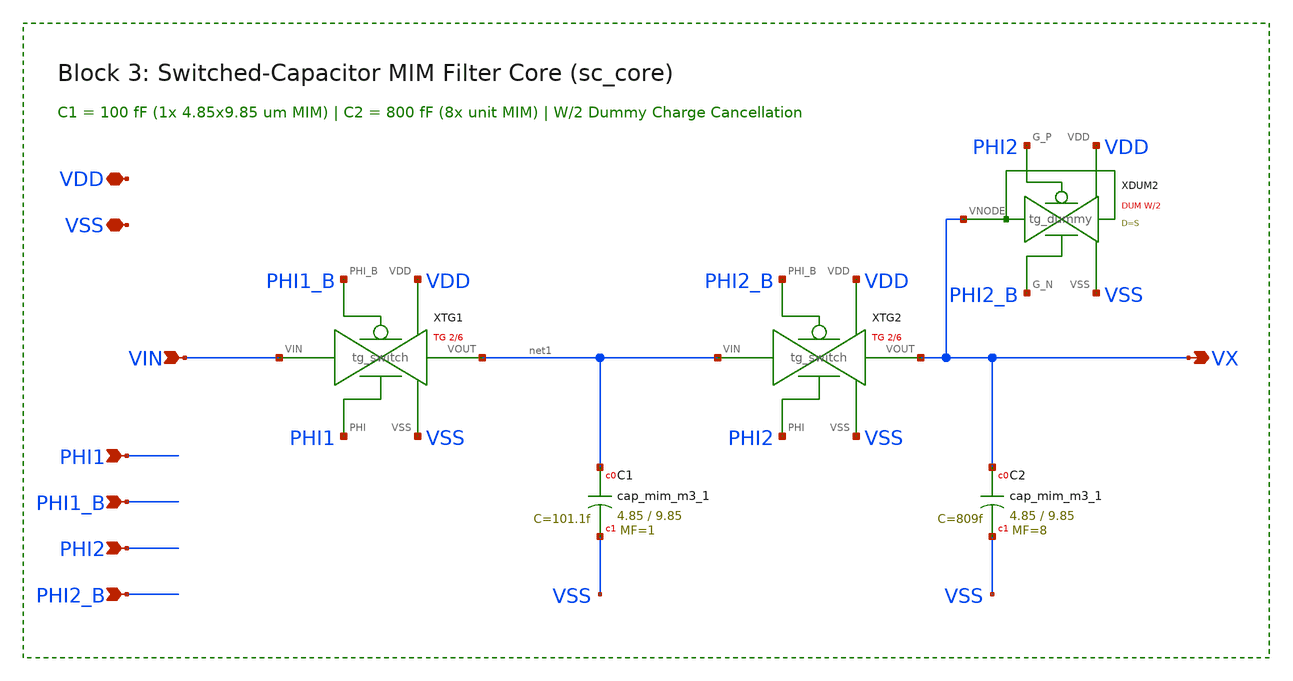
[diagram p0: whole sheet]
** sch_path: sky130-sc-lpf/xschem/sc_core.sch
**.subckt sc_core VDD VSS PHI1 PHI1_B PHI2 PHI2_B VIN VX
*.iopin VDD
*.iopin VSS
*.ipin PHI1
*.ipin PHI1_B
*.ipin PHI2
*.ipin PHI2_B
*.ipin VIN
*.opin VX
XTG1 VIN net1 PHI1 PHI1_B VDD VSS tg_switch
XC1 net1 VSS sky130_fd_pr__cap_mim_m3_1 W=4.85 L=9.85 MF=1 m=1
XTG2 net1 VX PHI2 PHI2_B VDD VSS tg_switch
XC2 VX VSS sky130_fd_pr__cap_mim_m3_1 W=4.85 L=9.85 MF=8 m=8
XDUM2 VX PHI2_B PHI2 VDD VSS tg_dummy
**.ends

* expanding   symbol:  tg_switch.sym # of pins=6
** sym_path: sky130-sc-lpf/xschem/tg_switch.sym
** sch_path: sky130-sc-lpf/xschem/tg_switch.sch
.subckt tg_switch VIN VOUT PHI PHI_B VDD VSS
*.iopin VIN
*.iopin VOUT
*.ipin PHI_B
*.ipin PHI
*.iopin VDD
*.iopin VSS
XMP VOUT PHI_B VIN VDD sky130_fd_pr__pfet_01v8 L=0.15 W=6.0 nf=2 ad='int((nf+1)/2) * W/nf * 0.29' as='int((nf+2)/2) * W/nf * 0.29'
+ pd='2*int((nf+1)/2) * (W/nf + 0.29)' ps='2*int((nf+2)/2) * (W/nf + 0.29)' nrd='0.29 / W' nrs='0.29 / W'
+ sa=0 sb=0 sd=0 mult=1 m=1
XMN VOUT PHI VIN VSS sky130_fd_pr__nfet_01v8 L=0.15 W=2.0 nf=1 ad='int((1 + 1)/2) * 2.0 / 1 * 0.29' as='int((1 + 2)/2) * 2.0 / 1 * 0.29'
+ pd='2*int((1 + 1)/2) * (2.0 / 1 + 0.29)' ps='2*int((1 + 2)/2) * (2.0 / 1 + 0.29)' nrd='0.29 / 2.0 ' nrs='0.29 / 2.0 '
+ sa=0 sb=0 sd=0 mult=1 m=1
.ends


* expanding   symbol:  tg_dummy.sym # of pins=5
** sym_path: sky130-sc-lpf/xschem/tg_dummy.sym
** sch_path: sky130-sc-lpf/xschem/tg_dummy.sch
.subckt tg_dummy VNODE G_N G_P VDD VSS
*.iopin VNODE
*.ipin G_P
*.ipin G_N
*.iopin VDD
*.iopin VSS
XMPD VNODE G_P VNODE VDD sky130_fd_pr__pfet_01v8 L=0.15 W=3.0 nf=1 ad='int((nf+1)/2) * W/nf * 0.29' as='int((nf+2)/2) * W/nf * 0.29'
+ pd='2*int((nf+1)/2) * (W/nf + 0.29)' ps='2*int((nf+2)/2) * (W/nf + 0.29)' nrd='0.29 / W' nrs='0.29 / W'
+ sa=0 sb=0 sd=0 mult=1 m=1
XMND VNODE G_N VNODE VSS sky130_fd_pr__nfet_01v8 L=0.15 W=1.0 nf=1 ad='int((1 + 1)/2) * 1.0 / 1 * 0.29'
+ as='int((1 + 2)/2) * 1.0 / 1 * 0.29' pd='2*int((1 + 1)/2) * (1.0 / 1 + 0.29)' ps='2*int((1 + 2)/2) * (1.0 / 1 + 0.29)'
+ nrd='0.29 / 1.0 ' nrs='0.29 / 1.0 ' sa=0 sb=0 sd=0 mult=1 m=1
.ends

.end
